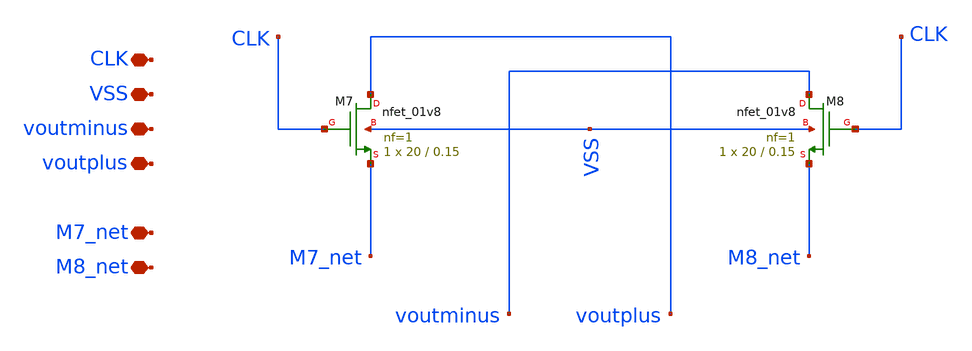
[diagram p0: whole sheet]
** sch_path: xschem/NMOS_5_6_test.sch
**.subckt NMOS_5_6_test CLK VSS voutminus voutplus M7_net M8_net
*.iopin CLK
*.iopin VSS
*.iopin voutminus
*.iopin voutplus
*.iopin M7_net
*.iopin M8_net
XM7 voutplus CLK M7_net VSS sky130_fd_pr__nfet_01v8 L=0.15 W=20 nf=1 ad='int((nf+1)/2) * W/nf * 0.29'
+ as='int((nf+2)/2) * W/nf * 0.29' pd='2*int((nf+1)/2) * (W/nf + 0.29)' ps='2*int((nf+2)/2) * (W/nf + 0.29)'
+ nrd='0.29 / W' nrs='0.29 / W' sa=0 sb=0 sd=0 mult=1 m=1
XM8 voutminus CLK M8_net VSS sky130_fd_pr__nfet_01v8 L=0.15 W=20 nf=1 ad='int((nf+1)/2) * W/nf * 0.29'
+ as='int((nf+2)/2) * W/nf * 0.29' pd='2*int((nf+1)/2) * (W/nf + 0.29)' ps='2*int((nf+2)/2) * (W/nf + 0.29)'
+ nrd='0.29 / W' nrs='0.29 / W' sa=0 sb=0 sd=0 mult=1 m=1
**.ends
.end
